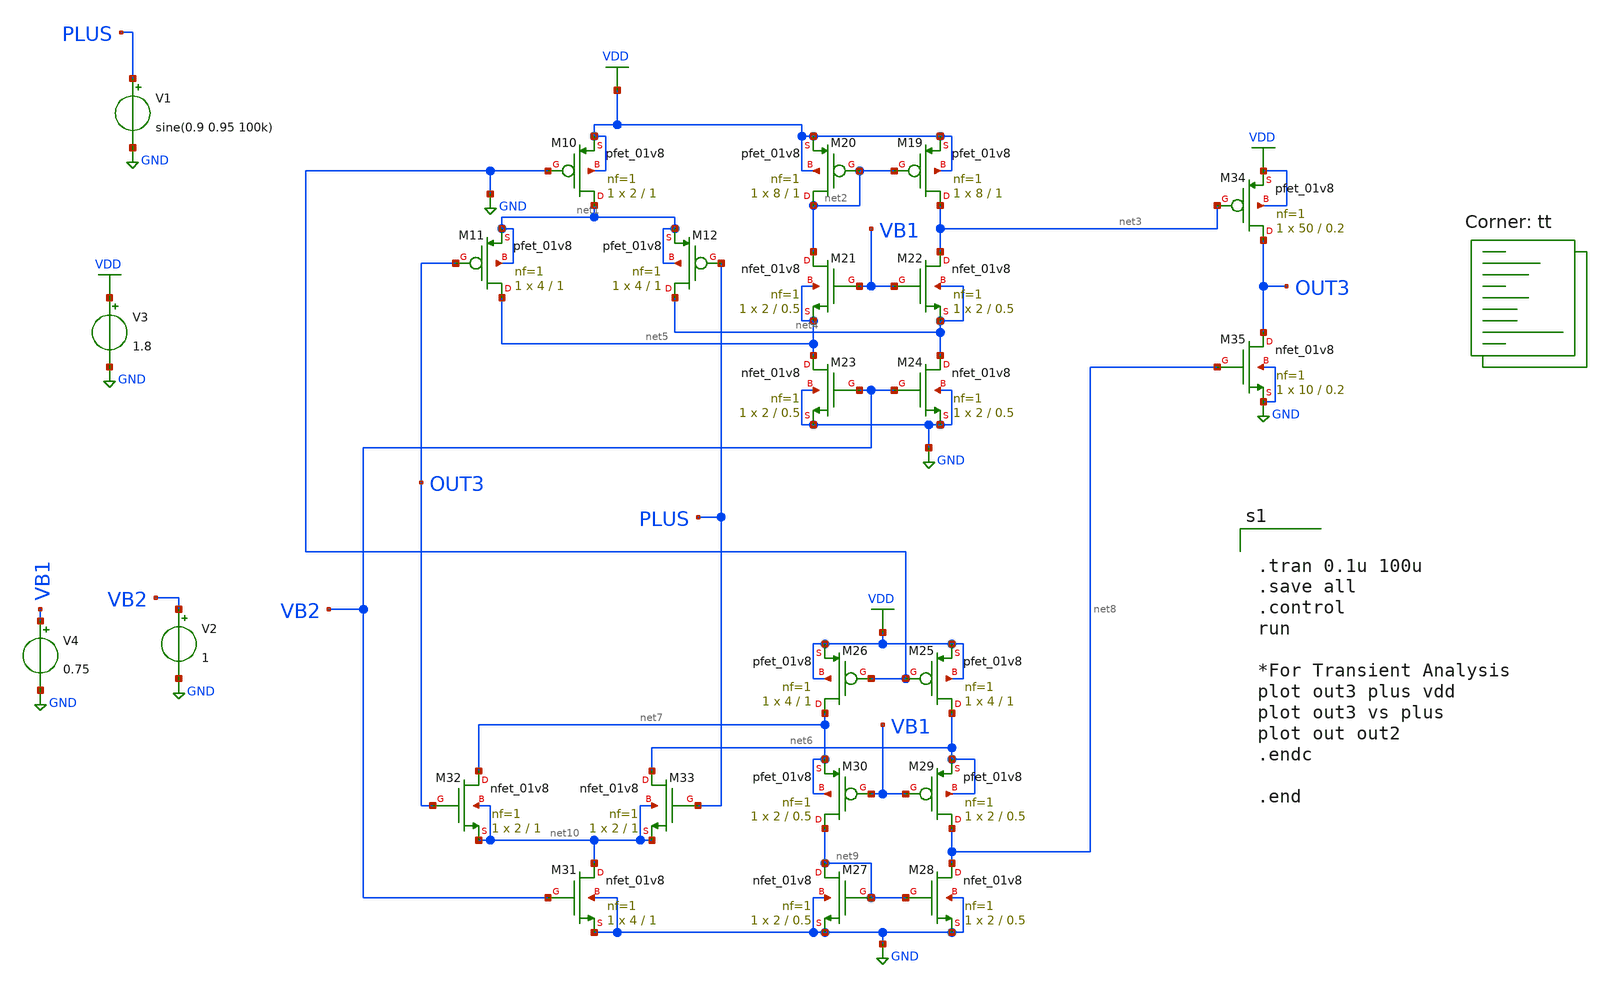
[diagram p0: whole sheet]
** sch_path: rail2rail_opamp/schematic/schem.sch
**.subckt schem
XM10 net1 GND VDD VDD sky130_fd_pr__pfet_01v8 L=1 W=2 nf=1 ad='int((nf+1)/2) * W/nf * 0.29' as='int((nf+2)/2) * W/nf * 0.29'
+ pd='2*int((nf+1)/2) * (W/nf + 0.29)' ps='2*int((nf+2)/2) * (W/nf + 0.29)' nrd='0.29 / W' nrs='0.29 / W'
+ sa=0 sb=0 sd=0 mult=1 m=1
XM11 net5 OUT3 net1 net1 sky130_fd_pr__pfet_01v8 L=1 W=4 nf=1 ad='int((nf+1)/2) * W/nf * 0.29' as='int((nf+2)/2) * W/nf * 0.29'
+ pd='2*int((nf+1)/2) * (W/nf + 0.29)' ps='2*int((nf+2)/2) * (W/nf + 0.29)' nrd='0.29 / W' nrs='0.29 / W'
+ sa=0 sb=0 sd=0 mult=1 m=1
XM12 net4 PLUS net1 net1 sky130_fd_pr__pfet_01v8 L=1 W=4 nf=1 ad='int((nf+1)/2) * W/nf * 0.29' as='int((nf+2)/2) * W/nf * 0.29'
+ pd='2*int((nf+1)/2) * (W/nf + 0.29)' ps='2*int((nf+2)/2) * (W/nf + 0.29)' nrd='0.29 / W' nrs='0.29 / W'
+ sa=0 sb=0 sd=0 mult=1 m=1
XM19 net3 net2 VDD VDD sky130_fd_pr__pfet_01v8 L=1 W=8 nf=1 ad='int((nf+1)/2) * W/nf * 0.29' as='int((nf+2)/2) * W/nf * 0.29'
+ pd='2*int((nf+1)/2) * (W/nf + 0.29)' ps='2*int((nf+2)/2) * (W/nf + 0.29)' nrd='0.29 / W' nrs='0.29 / W'
+ sa=0 sb=0 sd=0 mult=1 m=1
XM20 net2 net2 VDD VDD sky130_fd_pr__pfet_01v8 L=1 W=8 nf=1 ad='int((nf+1)/2) * W/nf * 0.29' as='int((nf+2)/2) * W/nf * 0.29'
+ pd='2*int((nf+1)/2) * (W/nf + 0.29)' ps='2*int((nf+2)/2) * (W/nf + 0.29)' nrd='0.29 / W' nrs='0.29 / W'
+ sa=0 sb=0 sd=0 mult=1 m=1
XM21 net2 VB1 net5 net5 sky130_fd_pr__nfet_01v8 L=0.5 W=2 nf=1 ad='int((nf+1)/2) * W/nf * 0.29' as='int((nf+2)/2) * W/nf * 0.29'
+ pd='2*int((nf+1)/2) * (W/nf + 0.29)' ps='2*int((nf+2)/2) * (W/nf + 0.29)' nrd='0.29 / W' nrs='0.29 / W'
+ sa=0 sb=0 sd=0 mult=1 m=1
XM22 net3 VB1 net4 net4 sky130_fd_pr__nfet_01v8 L=0.5 W=2 nf=1 ad='int((nf+1)/2) * W/nf * 0.29' as='int((nf+2)/2) * W/nf * 0.29'
+ pd='2*int((nf+1)/2) * (W/nf + 0.29)' ps='2*int((nf+2)/2) * (W/nf + 0.29)' nrd='0.29 / W' nrs='0.29 / W'
+ sa=0 sb=0 sd=0 mult=1 m=1
XM23 net5 VB2 GND GND sky130_fd_pr__nfet_01v8 L=0.5 W=2 nf=1 ad='int((nf+1)/2) * W/nf * 0.29' as='int((nf+2)/2) * W/nf * 0.29'
+ pd='2*int((nf+1)/2) * (W/nf + 0.29)' ps='2*int((nf+2)/2) * (W/nf + 0.29)' nrd='0.29 / W' nrs='0.29 / W'
+ sa=0 sb=0 sd=0 mult=1 m=1
XM24 net4 VB2 GND GND sky130_fd_pr__nfet_01v8 L=0.5 W=2 nf=1 ad='int((nf+1)/2) * W/nf * 0.29' as='int((nf+2)/2) * W/nf * 0.29'
+ pd='2*int((nf+1)/2) * (W/nf + 0.29)' ps='2*int((nf+2)/2) * (W/nf + 0.29)' nrd='0.29 / W' nrs='0.29 / W'
+ sa=0 sb=0 sd=0 mult=1 m=1
XM25 net6 GND VDD VDD sky130_fd_pr__pfet_01v8 L=1 W=4 nf=1 ad='int((nf+1)/2) * W/nf * 0.29' as='int((nf+2)/2) * W/nf * 0.29'
+ pd='2*int((nf+1)/2) * (W/nf + 0.29)' ps='2*int((nf+2)/2) * (W/nf + 0.29)' nrd='0.29 / W' nrs='0.29 / W'
+ sa=0 sb=0 sd=0 mult=1 m=1
XM26 net7 GND VDD VDD sky130_fd_pr__pfet_01v8 L=1 W=4 nf=1 ad='int((nf+1)/2) * W/nf * 0.29' as='int((nf+2)/2) * W/nf * 0.29'
+ pd='2*int((nf+1)/2) * (W/nf + 0.29)' ps='2*int((nf+2)/2) * (W/nf + 0.29)' nrd='0.29 / W' nrs='0.29 / W'
+ sa=0 sb=0 sd=0 mult=1 m=1
XM27 net9 net9 GND GND sky130_fd_pr__nfet_01v8 L=0.5 W=2 nf=1 ad='int((nf+1)/2) * W/nf * 0.29' as='int((nf+2)/2) * W/nf * 0.29'
+ pd='2*int((nf+1)/2) * (W/nf + 0.29)' ps='2*int((nf+2)/2) * (W/nf + 0.29)' nrd='0.29 / W' nrs='0.29 / W'
+ sa=0 sb=0 sd=0 mult=1 m=1
XM28 net8 net9 GND GND sky130_fd_pr__nfet_01v8 L=0.5 W=2 nf=1 ad='int((nf+1)/2) * W/nf * 0.29' as='int((nf+2)/2) * W/nf * 0.29'
+ pd='2*int((nf+1)/2) * (W/nf + 0.29)' ps='2*int((nf+2)/2) * (W/nf + 0.29)' nrd='0.29 / W' nrs='0.29 / W'
+ sa=0 sb=0 sd=0 mult=1 m=1
XM29 net8 VB1 net6 net6 sky130_fd_pr__pfet_01v8 L=0.5 W=2 nf=1 ad='int((nf+1)/2) * W/nf * 0.29' as='int((nf+2)/2) * W/nf * 0.29'
+ pd='2*int((nf+1)/2) * (W/nf + 0.29)' ps='2*int((nf+2)/2) * (W/nf + 0.29)' nrd='0.29 / W' nrs='0.29 / W'
+ sa=0 sb=0 sd=0 mult=1 m=1
XM30 net9 VB1 net7 net7 sky130_fd_pr__pfet_01v8 L=0.5 W=2 nf=1 ad='int((nf+1)/2) * W/nf * 0.29' as='int((nf+2)/2) * W/nf * 0.29'
+ pd='2*int((nf+1)/2) * (W/nf + 0.29)' ps='2*int((nf+2)/2) * (W/nf + 0.29)' nrd='0.29 / W' nrs='0.29 / W'
+ sa=0 sb=0 sd=0 mult=1 m=1
XM31 net10 VB2 GND GND sky130_fd_pr__nfet_01v8 L=1 W=4 nf=1 ad='int((nf+1)/2) * W/nf * 0.29' as='int((nf+2)/2) * W/nf * 0.29'
+ pd='2*int((nf+1)/2) * (W/nf + 0.29)' ps='2*int((nf+2)/2) * (W/nf + 0.29)' nrd='0.29 / W' nrs='0.29 / W'
+ sa=0 sb=0 sd=0 mult=1 m=1
XM32 net7 OUT3 net10 net10 sky130_fd_pr__nfet_01v8 L=1 W=2 nf=1 ad='int((nf+1)/2) * W/nf * 0.29' as='int((nf+2)/2) * W/nf * 0.29'
+ pd='2*int((nf+1)/2) * (W/nf + 0.29)' ps='2*int((nf+2)/2) * (W/nf + 0.29)' nrd='0.29 / W' nrs='0.29 / W'
+ sa=0 sb=0 sd=0 mult=1 m=1
XM33 net6 PLUS net10 net10 sky130_fd_pr__nfet_01v8 L=1 W=2 nf=1 ad='int((nf+1)/2) * W/nf * 0.29' as='int((nf+2)/2) * W/nf * 0.29'
+ pd='2*int((nf+1)/2) * (W/nf + 0.29)' ps='2*int((nf+2)/2) * (W/nf + 0.29)' nrd='0.29 / W' nrs='0.29 / W'
+ sa=0 sb=0 sd=0 mult=1 m=1
XM34 OUT3 net3 VDD VDD sky130_fd_pr__pfet_01v8 L=0.2 W=50 nf=1 ad='int((nf+1)/2) * W/nf * 0.29' as='int((nf+2)/2) * W/nf * 0.29'
+ pd='2*int((nf+1)/2) * (W/nf + 0.29)' ps='2*int((nf+2)/2) * (W/nf + 0.29)' nrd='0.29 / W' nrs='0.29 / W'
+ sa=0 sb=0 sd=0 mult=1 m=1
XM35 OUT3 net8 GND GND sky130_fd_pr__nfet_01v8 L=0.2 W=10 nf=1 ad='int((nf+1)/2) * W/nf * 0.29' as='int((nf+2)/2) * W/nf * 0.29'
+ pd='2*int((nf+1)/2) * (W/nf + 0.29)' ps='2*int((nf+2)/2) * (W/nf + 0.29)' nrd='0.29 / W' nrs='0.29 / W'
+ sa=0 sb=0 sd=0 mult=1 m=1
V1 PLUS GND sine(0.9 0.95 100k)
V3 VDD GND 1.8
V2 VB2 GND 1
V4 VB1 GND 0.75
**** begin user architecture code
.lib $::SKYWATER_MODELS/sky130.lib.spice tt


.tran 0.1u 100u
.save all
.control
run

*For Transient Analysis
plot out3 plus vdd
plot out3 vs plus
plot out out2
.endc

.end


**** end user architecture code
**.ends
.GLOBAL VDD
.GLOBAL GND
.end
